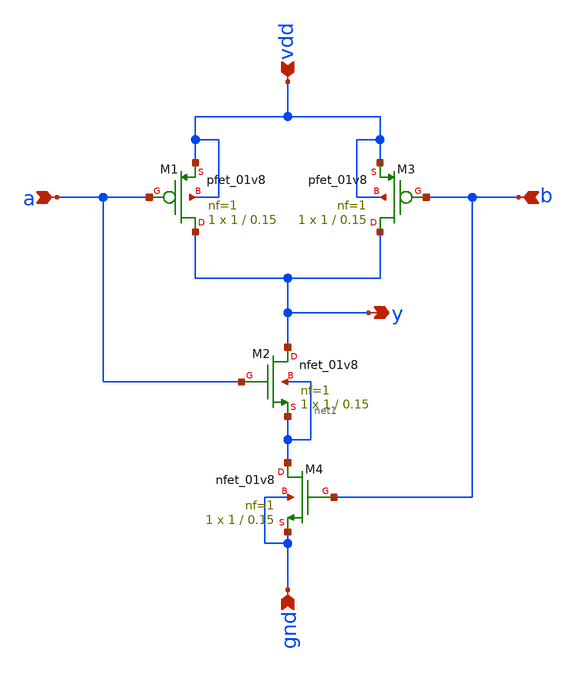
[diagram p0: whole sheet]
** sch_path: sram/nand_gate.sch
**.subckt nand_gate a b vdd gnd y
*.ipin a
*.ipin b
*.ipin vdd
*.ipin gnd
*.opin y
XM1 y a vdd vdd sky130_fd_pr__pfet_01v8 L=0.15 W=1 nf=1 ad='int((nf+1)/2) * W/nf * 0.29' as='int((nf+2)/2) * W/nf * 0.29'
+ pd='2*int((nf+1)/2) * (W/nf + 0.29)' ps='2*int((nf+2)/2) * (W/nf + 0.29)' nrd='0.29 / W' nrs='0.29 / W'
+ sa=0 sb=0 sd=0 mult=1 m=1
XM2 y a net1 net1 sky130_fd_pr__nfet_01v8 L=0.15 W=1 nf=1 ad='int((nf+1)/2) * W/nf * 0.29' as='int((nf+2)/2) * W/nf * 0.29'
+ pd='2*int((nf+1)/2) * (W/nf + 0.29)' ps='2*int((nf+2)/2) * (W/nf + 0.29)' nrd='0.29 / W' nrs='0.29 / W'
+ sa=0 sb=0 sd=0 mult=1 m=1
XM3 y b vdd vdd sky130_fd_pr__pfet_01v8 L=0.15 W=1 nf=1 ad='int((nf+1)/2) * W/nf * 0.29' as='int((nf+2)/2) * W/nf * 0.29'
+ pd='2*int((nf+1)/2) * (W/nf + 0.29)' ps='2*int((nf+2)/2) * (W/nf + 0.29)' nrd='0.29 / W' nrs='0.29 / W'
+ sa=0 sb=0 sd=0 mult=1 m=1
XM4 net1 b gnd gnd sky130_fd_pr__nfet_01v8 L=0.15 W=1 nf=1 ad='int((nf+1)/2) * W/nf * 0.29' as='int((nf+2)/2) * W/nf * 0.29'
+ pd='2*int((nf+1)/2) * (W/nf + 0.29)' ps='2*int((nf+2)/2) * (W/nf + 0.29)' nrd='0.29 / W' nrs='0.29 / W'
+ sa=0 sb=0 sd=0 mult=1 m=1
**.ends
.end
